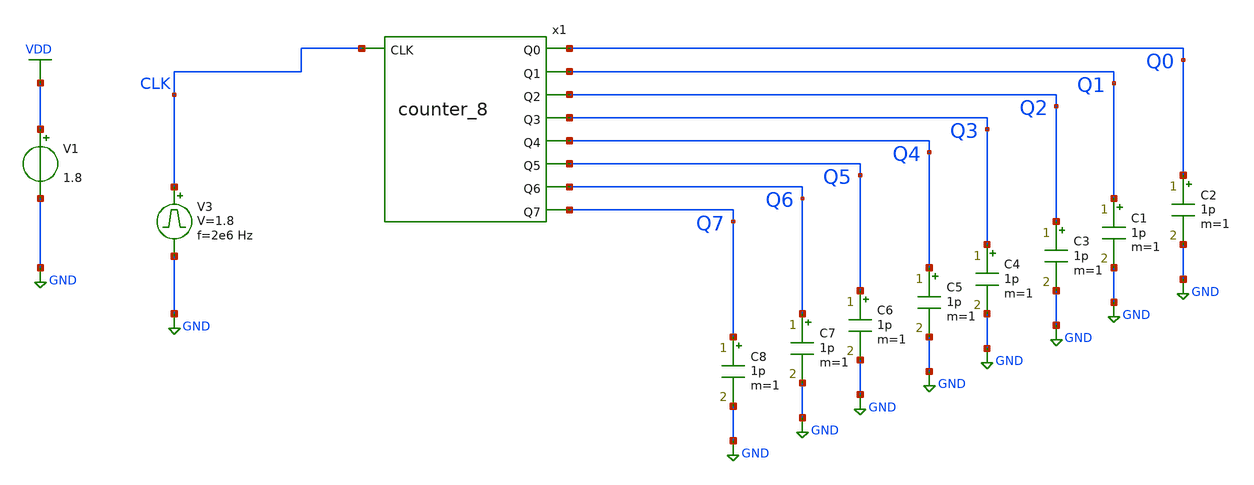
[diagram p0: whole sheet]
** sch_path: circuits/xschem/counter_8_tb.sch
**.subckt counter_8_tb
V1 VDD GND 1.8
V3 CLK GND pulse 0 1.8 '0.495/ 2e6 ' '0.01/2e6 ' '0.01/2e6 ' '0.49/2e6 ' '1/2e6 '
C2 Q0 GND 1p m=1
x1 Q0 Q1 Q2 Q3 Q4 Q5 Q6 Q7 CLK counter_8
C1 Q1 GND 1p m=1
C3 Q2 GND 1p m=1
C4 Q3 GND 1p m=1
C5 Q4 GND 1p m=1
C6 Q5 GND 1p m=1
C7 Q6 GND 1p m=1
C8 Q7 GND 1p m=1
**** begin user architecture code


.control
save all
tran 1n 80u
plot V(CLK) V(Q0)+2 V(Q1)+4 V(Q2)+6 V(Q3)+8 V(Q4)+10 V(Q5)+12 V(Q6)+14 V(Q7)+16
.endc



** opencircuitdesign pdks install
.lib $::SKYWATER_MODELS/sky130.lib.spice tt


**** end user architecture code
**.ends
.GLOBAL VDD
.GLOBAL GND
.end
